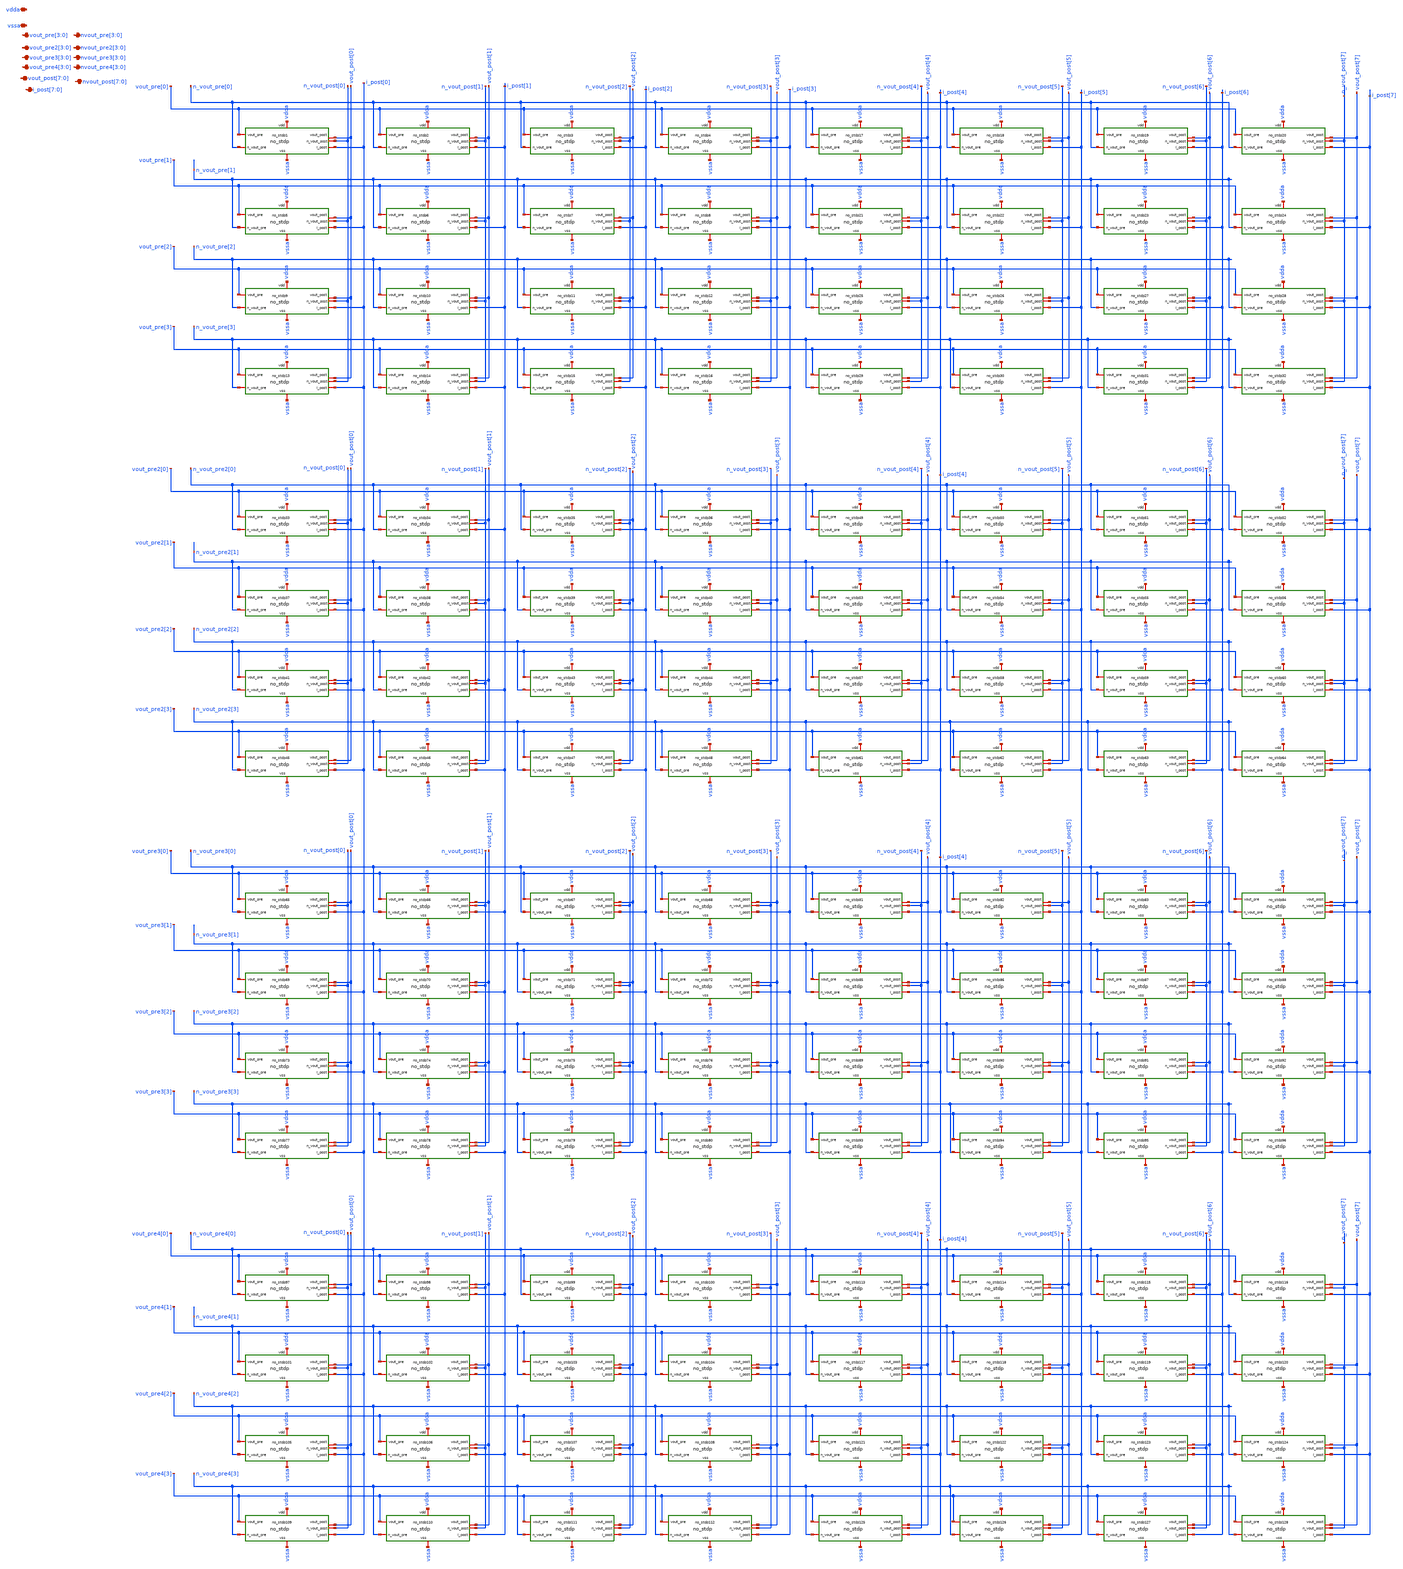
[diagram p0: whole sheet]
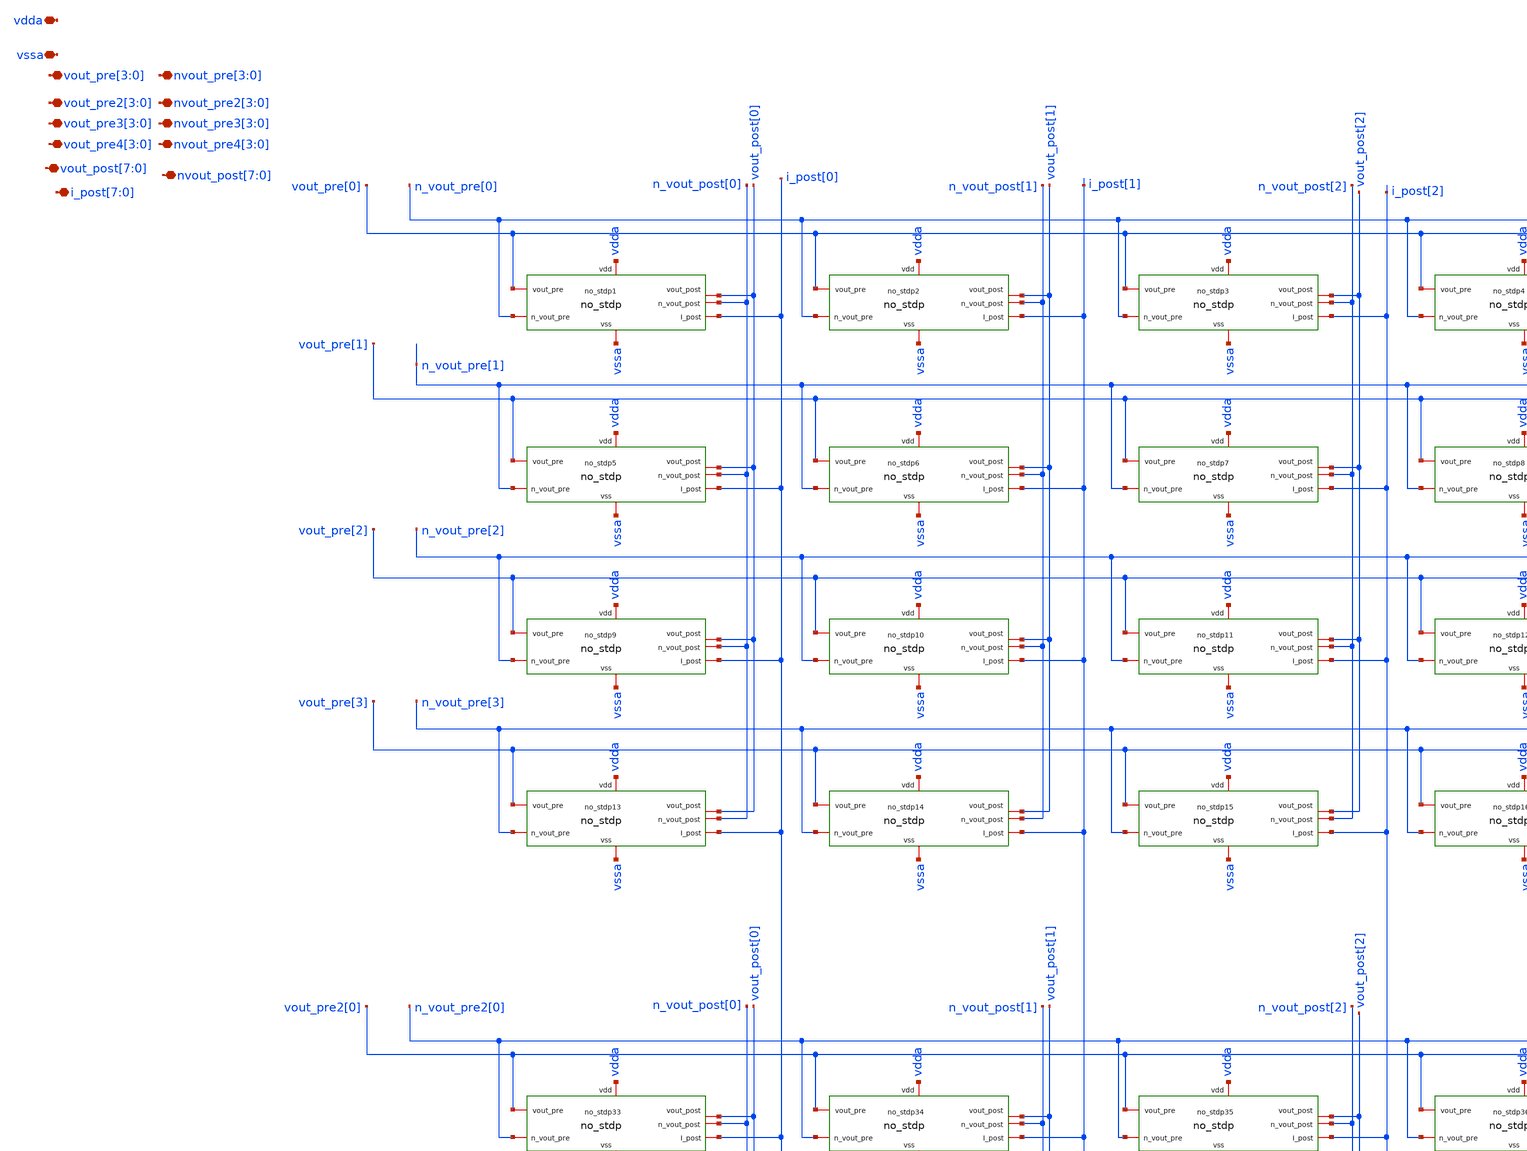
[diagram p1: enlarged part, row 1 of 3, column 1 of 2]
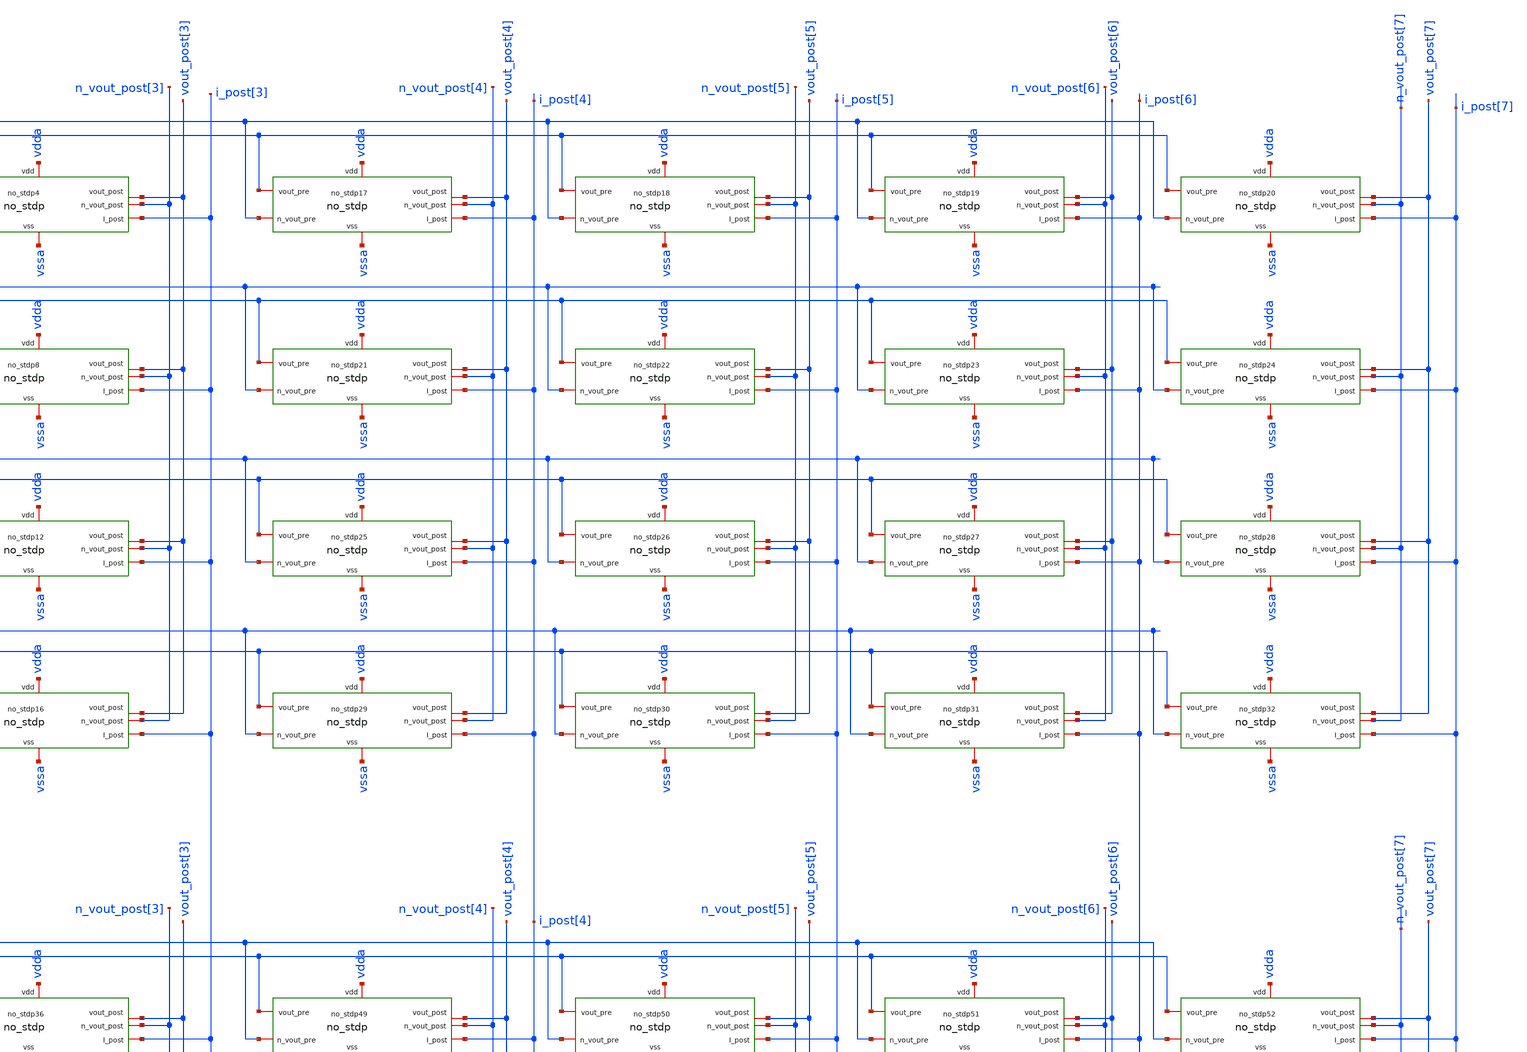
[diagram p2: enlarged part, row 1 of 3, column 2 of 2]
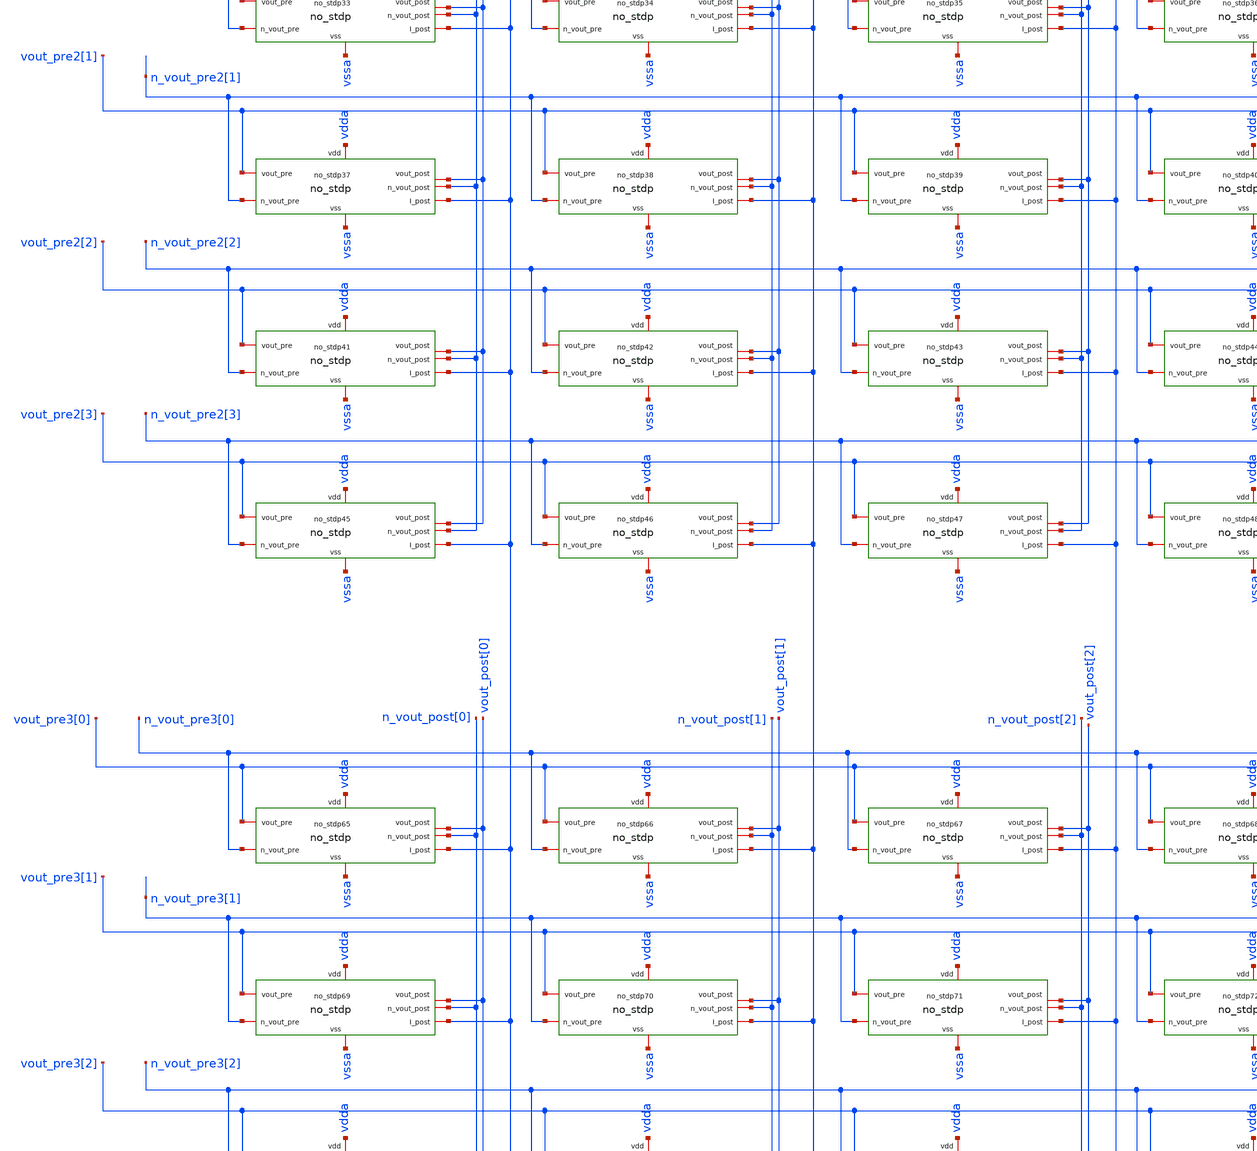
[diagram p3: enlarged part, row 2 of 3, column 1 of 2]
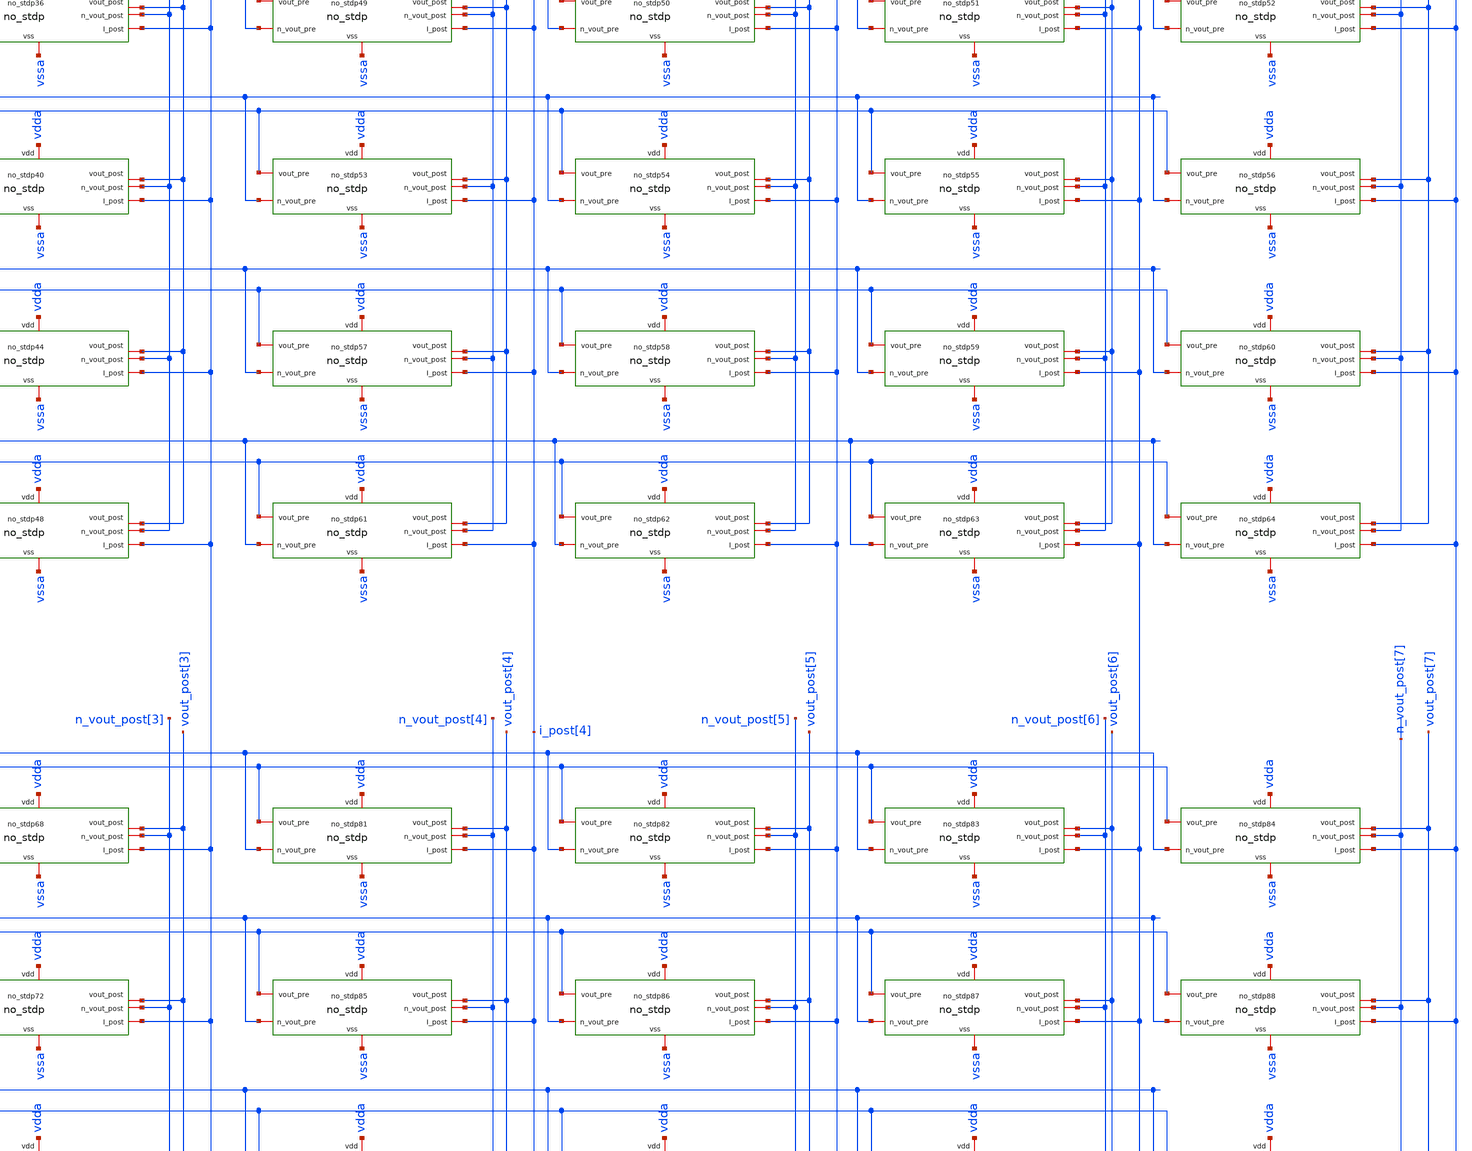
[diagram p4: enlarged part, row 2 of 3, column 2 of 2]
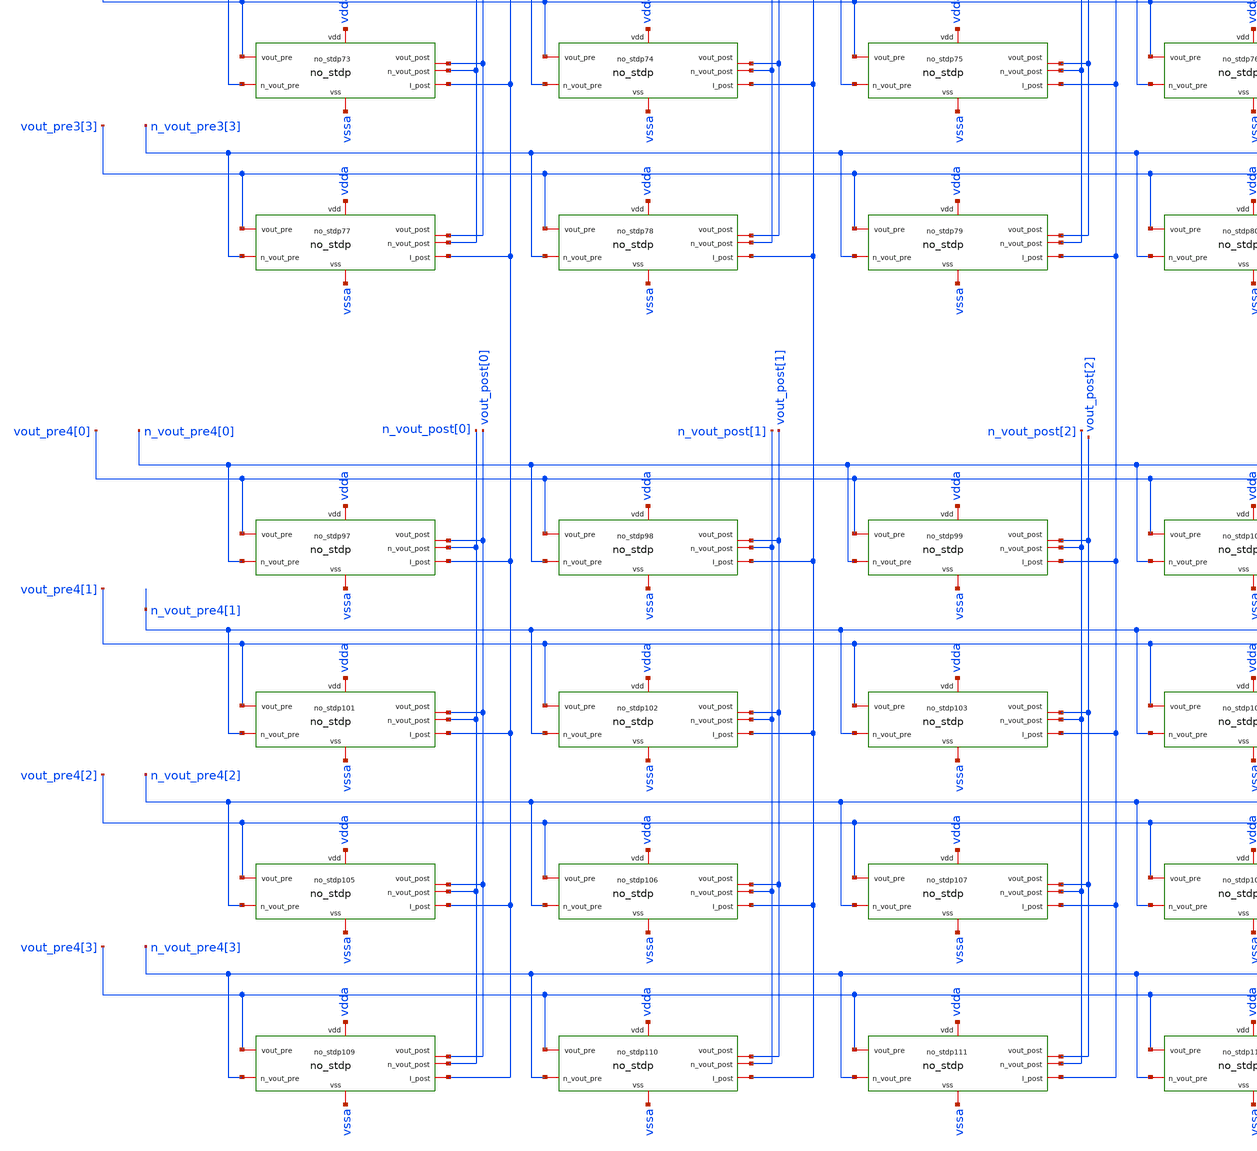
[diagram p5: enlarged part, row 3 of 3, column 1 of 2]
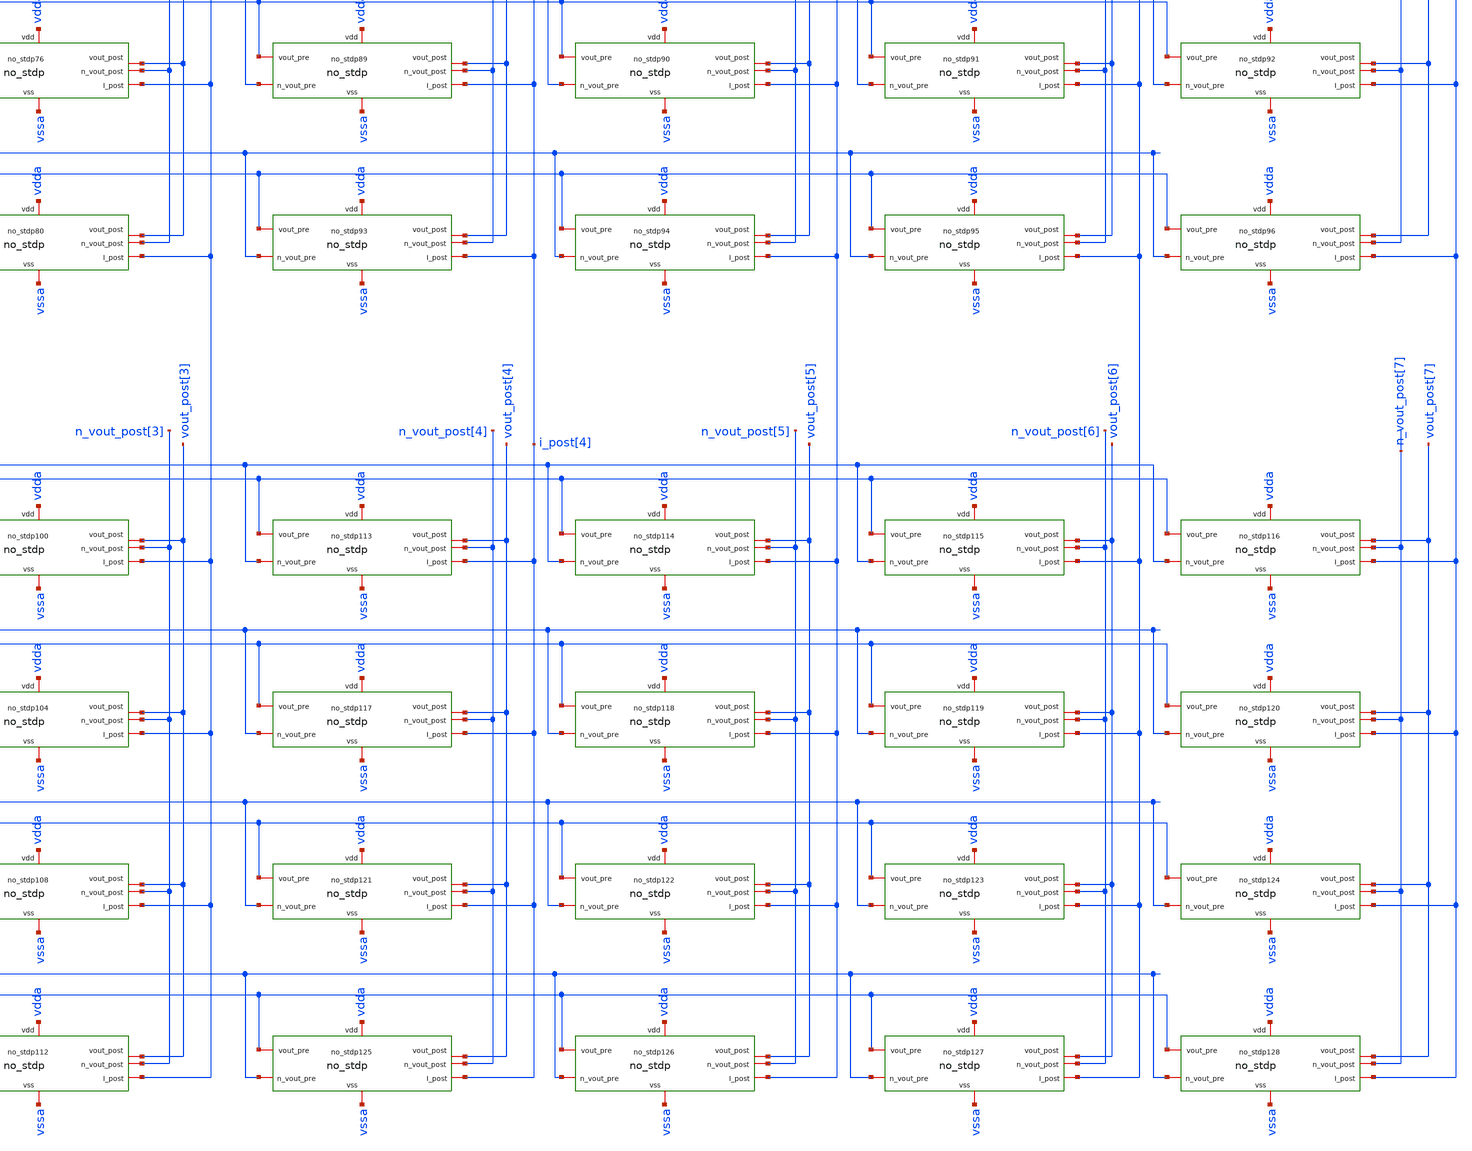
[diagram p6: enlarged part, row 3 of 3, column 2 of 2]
** sch_path: Synapse/no_stdp_4x4x8.sch
**.subckt no_stdp_4x4x8 vdda vssa vout_pre[3],vout_pre[2],vout_pre[1],vout_pre[0]
*+ vout_post[7],vout_post[6],vout_post[5],vout_post[4],vout_post[3],vout_post[2],vout_post[1],vout_post[0] i_post[7],i_post[6],i_post[5],i_post[4],i_post[3],i_post[2],i_post[1],i_post[0]
*+ vout_pre2[3],vout_pre2[2],vout_pre2[1],vout_pre2[0] vout_pre3[3],vout_pre3[2],vout_pre3[1],vout_pre3[0]
*+ vout_pre4[3],vout_pre4[2],vout_pre4[1],vout_pre4[0] nvout_pre[3],nvout_pre[2],nvout_pre[1],nvout_pre[0]
*+ nvout_pre2[3],nvout_pre2[2],nvout_pre2[1],nvout_pre2[0] nvout_pre3[3],nvout_pre3[2],nvout_pre3[1],nvout_pre3[0]
*+ nvout_pre4[3],nvout_pre4[2],nvout_pre4[1],nvout_pre4[0]
*+ nvout_post[7],nvout_post[6],nvout_post[5],nvout_post[4],nvout_post[3],nvout_post[2],nvout_post[1],nvout_post[0]
*.iopin vdda
*.iopin vssa
*.iopin vout_pre[3],vout_pre[2],vout_pre[1],vout_pre[0]
*.iopin
*+ vout_post[7],vout_post[6],vout_post[5],vout_post[4],vout_post[3],vout_post[2],vout_post[1],vout_post[0]
*.iopin i_post[7],i_post[6],i_post[5],i_post[4],i_post[3],i_post[2],i_post[1],i_post[0]
*.iopin vout_pre2[3],vout_pre2[2],vout_pre2[1],vout_pre2[0]
*.iopin vout_pre3[3],vout_pre3[2],vout_pre3[1],vout_pre3[0]
*.iopin vout_pre4[3],vout_pre4[2],vout_pre4[1],vout_pre4[0]
*.iopin nvout_pre[3],nvout_pre[2],nvout_pre[1],nvout_pre[0]
*.iopin nvout_pre2[3],nvout_pre2[2],nvout_pre2[1],nvout_pre2[0]
*.iopin nvout_pre3[3],nvout_pre3[2],nvout_pre3[1],nvout_pre3[0]
*.iopin nvout_pre4[3],nvout_pre4[2],nvout_pre4[1],nvout_pre4[0]
*.iopin
*+ nvout_post[7],nvout_post[6],nvout_post[5],nvout_post[4],nvout_post[3],nvout_post[2],nvout_post[1],nvout_post[0]
xno_stdp1 vdda vssa vout_pre[0] vout_post[0] i_post[0] n_vout_pre[0] n_vout_post[0] no_stdp
xno_stdp2 vdda vssa vout_pre[0] vout_post[1] i_post[1] n_vout_pre[0] n_vout_post[1] no_stdp
xno_stdp3 vdda vssa vout_pre[0] vout_post[2] i_post[2] n_vout_pre[0] n_vout_post[2] no_stdp
xno_stdp4 vdda vssa vout_pre[0] vout_post[3] i_post[3] n_vout_pre[0] n_vout_post[3] no_stdp
xno_stdp5 vdda vssa vout_pre[1] vout_post[0] i_post[0] n_vout_pre[1] n_vout_post[0] no_stdp
xno_stdp6 vdda vssa vout_pre[1] vout_post[1] i_post[1] n_vout_pre[1] n_vout_post[1] no_stdp
xno_stdp7 vdda vssa vout_pre[1] vout_post[2] i_post[2] n_vout_pre[1] n_vout_post[2] no_stdp
xno_stdp8 vdda vssa vout_pre[1] vout_post[3] i_post[3] n_vout_pre[1] n_vout_post[3] no_stdp
xno_stdp9 vdda vssa vout_pre[2] vout_post[0] i_post[0] n_vout_pre[2] n_vout_post[0] no_stdp
xno_stdp10 vdda vssa vout_pre[2] vout_post[1] i_post[1] n_vout_pre[2] n_vout_post[1] no_stdp
xno_stdp11 vdda vssa vout_pre[2] vout_post[2] i_post[2] n_vout_pre[2] n_vout_post[2] no_stdp
xno_stdp12 vdda vssa vout_pre[2] vout_post[3] i_post[3] n_vout_pre[2] n_vout_post[3] no_stdp
xno_stdp13 vdda vssa vout_pre[3] vout_post[0] i_post[0] n_vout_pre[3] n_vout_post[0] no_stdp
xno_stdp14 vdda vssa vout_pre[3] vout_post[1] i_post[1] n_vout_pre[3] n_vout_post[1] no_stdp
xno_stdp15 vdda vssa vout_pre[3] vout_post[2] i_post[2] n_vout_pre[3] n_vout_post[2] no_stdp
xno_stdp16 vdda vssa vout_pre[3] vout_post[3] i_post[3] n_vout_pre[3] n_vout_post[3] no_stdp
xno_stdp17 vdda vssa vout_pre[0] vout_post[4] i_post[4] n_vout_pre[0] n_vout_post[4] no_stdp
xno_stdp18 vdda vssa vout_pre[0] vout_post[5] i_post[5] n_vout_pre[0] n_vout_post[5] no_stdp
xno_stdp19 vdda vssa vout_pre[0] vout_post[6] i_post[6] n_vout_pre[0] n_vout_post[6] no_stdp
xno_stdp20 vdda vssa vout_pre[0] vout_post[7] i_post[7] n_vout_pre[0] n_vout_post[7] no_stdp
xno_stdp21 vdda vssa vout_pre[1] vout_post[4] i_post[4] n_vout_pre[1] n_vout_post[4] no_stdp
xno_stdp22 vdda vssa vout_pre[1] vout_post[5] i_post[5] n_vout_pre[1] n_vout_post[5] no_stdp
xno_stdp23 vdda vssa vout_pre[1] vout_post[6] i_post[6] n_vout_pre[1] n_vout_post[6] no_stdp
xno_stdp24 vdda vssa vout_pre[1] vout_post[7] i_post[7] n_vout_pre[1] n_vout_post[7] no_stdp
xno_stdp25 vdda vssa vout_pre[2] vout_post[4] i_post[4] n_vout_pre[2] n_vout_post[4] no_stdp
xno_stdp26 vdda vssa vout_pre[2] vout_post[5] i_post[5] n_vout_pre[2] n_vout_post[5] no_stdp
xno_stdp27 vdda vssa vout_pre[2] vout_post[6] i_post[6] n_vout_pre[2] n_vout_post[6] no_stdp
xno_stdp28 vdda vssa vout_pre[2] vout_post[7] i_post[7] n_vout_pre[2] n_vout_post[7] no_stdp
xno_stdp29 vdda vssa vout_pre[3] vout_post[4] i_post[4] n_vout_pre[3] n_vout_post[4] no_stdp
xno_stdp30 vdda vssa vout_pre[3] vout_post[5] i_post[5] n_vout_pre[3] n_vout_post[5] no_stdp
xno_stdp31 vdda vssa vout_pre[3] vout_post[6] i_post[6] n_vout_pre[3] n_vout_post[6] no_stdp
xno_stdp32 vdda vssa vout_pre[3] vout_post[7] i_post[7] n_vout_pre[3] n_vout_post[7] no_stdp
xno_stdp33 vdda vssa vout_pre2[0] vout_post[0] i_post[0] n_vout_pre2[0] n_vout_post[0] no_stdp
xno_stdp34 vdda vssa vout_pre2[0] vout_post[1] i_post[1] n_vout_pre2[0] n_vout_post[1] no_stdp
xno_stdp35 vdda vssa vout_pre2[0] vout_post[2] i_post[2] n_vout_pre2[0] n_vout_post[2] no_stdp
xno_stdp36 vdda vssa vout_pre2[0] vout_post[3] i_post[3] n_vout_pre2[0] n_vout_post[3] no_stdp
xno_stdp37 vdda vssa vout_pre2[1] vout_post[0] i_post[0] n_vout_pre2[1] n_vout_post[0] no_stdp
xno_stdp38 vdda vssa vout_pre2[1] vout_post[1] i_post[1] n_vout_pre2[1] n_vout_post[1] no_stdp
xno_stdp39 vdda vssa vout_pre2[1] vout_post[2] i_post[2] n_vout_pre2[1] n_vout_post[2] no_stdp
xno_stdp40 vdda vssa vout_pre2[1] vout_post[3] i_post[3] n_vout_pre2[1] n_vout_post[3] no_stdp
xno_stdp41 vdda vssa vout_pre2[2] vout_post[0] i_post[0] n_vout_pre2[2] n_vout_post[0] no_stdp
xno_stdp42 vdda vssa vout_pre2[2] vout_post[1] i_post[1] n_vout_pre2[2] n_vout_post[1] no_stdp
xno_stdp43 vdda vssa vout_pre2[2] vout_post[2] i_post[2] n_vout_pre2[2] n_vout_post[2] no_stdp
xno_stdp44 vdda vssa vout_pre2[2] vout_post[3] i_post[3] n_vout_pre2[2] n_vout_post[3] no_stdp
xno_stdp45 vdda vssa vout_pre2[3] vout_post[0] i_post[0] n_vout_pre2[3] n_vout_post[0] no_stdp
xno_stdp46 vdda vssa vout_pre2[3] vout_post[1] i_post[1] n_vout_pre2[3] n_vout_post[1] no_stdp
xno_stdp47 vdda vssa vout_pre2[3] vout_post[2] i_post[2] n_vout_pre2[3] n_vout_post[2] no_stdp
xno_stdp48 vdda vssa vout_pre2[3] vout_post[3] i_post[3] n_vout_pre2[3] n_vout_post[3] no_stdp
xno_stdp49 vdda vssa vout_pre2[0] vout_post[4] i_post[4] n_vout_pre2[0] n_vout_post[4] no_stdp
xno_stdp50 vdda vssa vout_pre2[0] vout_post[5] i_post[5] n_vout_pre2[0] n_vout_post[5] no_stdp
xno_stdp51 vdda vssa vout_pre2[0] vout_post[6] i_post[6] n_vout_pre2[0] n_vout_post[6] no_stdp
xno_stdp52 vdda vssa vout_pre2[0] vout_post[7] i_post[7] n_vout_pre2[0] n_vout_post[7] no_stdp
xno_stdp53 vdda vssa vout_pre2[1] vout_post[4] i_post[4] n_vout_pre2[1] n_vout_post[4] no_stdp
xno_stdp54 vdda vssa vout_pre2[1] vout_post[5] i_post[5] n_vout_pre2[1] n_vout_post[5] no_stdp
xno_stdp55 vdda vssa vout_pre2[1] vout_post[6] i_post[6] n_vout_pre2[1] n_vout_post[6] no_stdp
xno_stdp56 vdda vssa vout_pre2[1] vout_post[7] i_post[7] n_vout_pre2[1] n_vout_post[7] no_stdp
xno_stdp57 vdda vssa vout_pre2[2] vout_post[4] i_post[4] n_vout_pre2[2] n_vout_post[4] no_stdp
xno_stdp58 vdda vssa vout_pre2[2] vout_post[5] i_post[5] n_vout_pre2[2] n_vout_post[5] no_stdp
xno_stdp59 vdda vssa vout_pre2[2] vout_post[6] i_post[6] n_vout_pre2[2] n_vout_post[6] no_stdp
xno_stdp60 vdda vssa vout_pre2[2] vout_post[7] i_post[7] n_vout_pre2[2] n_vout_post[7] no_stdp
xno_stdp61 vdda vssa vout_pre2[3] vout_post[4] i_post[4] n_vout_pre2[3] n_vout_post[4] no_stdp
xno_stdp62 vdda vssa vout_pre2[3] vout_post[5] i_post[5] n_vout_pre2[3] n_vout_post[5] no_stdp
xno_stdp63 vdda vssa vout_pre2[3] vout_post[6] i_post[6] n_vout_pre2[3] n_vout_post[6] no_stdp
xno_stdp64 vdda vssa vout_pre2[3] vout_post[7] i_post[7] n_vout_pre2[3] n_vout_post[7] no_stdp
xno_stdp65 vdda vssa vout_pre3[0] vout_post[0] i_post[0] n_vout_pre3[0] n_vout_post[0] no_stdp
xno_stdp66 vdda vssa vout_pre3[0] vout_post[1] i_post[1] n_vout_pre3[0] n_vout_post[1] no_stdp
xno_stdp67 vdda vssa vout_pre3[0] vout_post[2] i_post[2] n_vout_pre3[0] n_vout_post[2] no_stdp
xno_stdp68 vdda vssa vout_pre3[0] vout_post[3] i_post[3] n_vout_pre3[0] n_vout_post[3] no_stdp
xno_stdp69 vdda vssa vout_pre3[1] vout_post[0] i_post[0] n_vout_pre3[1] n_vout_post[0] no_stdp
xno_stdp70 vdda vssa vout_pre3[1] vout_post[1] i_post[1] n_vout_pre3[1] n_vout_post[1] no_stdp
xno_stdp71 vdda vssa vout_pre3[1] vout_post[2] i_post[2] n_vout_pre3[1] n_vout_post[2] no_stdp
xno_stdp72 vdda vssa vout_pre3[1] vout_post[3] i_post[3] n_vout_pre3[1] n_vout_post[3] no_stdp
xno_stdp73 vdda vssa vout_pre3[2] vout_post[0] i_post[0] n_vout_pre3[2] n_vout_post[0] no_stdp
xno_stdp74 vdda vssa vout_pre3[2] vout_post[1] i_post[1] n_vout_pre3[2] n_vout_post[1] no_stdp
xno_stdp75 vdda vssa vout_pre3[2] vout_post[2] i_post[2] n_vout_pre3[2] n_vout_post[2] no_stdp
xno_stdp76 vdda vssa vout_pre3[2] vout_post[3] i_post[3] n_vout_pre3[2] n_vout_post[3] no_stdp
xno_stdp77 vdda vssa vout_pre3[3] vout_post[0] i_post[0] n_vout_pre3[3] n_vout_post[0] no_stdp
xno_stdp78 vdda vssa vout_pre3[3] vout_post[1] i_post[1] n_vout_pre3[3] n_vout_post[1] no_stdp
xno_stdp79 vdda vssa vout_pre3[3] vout_post[2] i_post[2] n_vout_pre3[3] n_vout_post[2] no_stdp
xno_stdp80 vdda vssa vout_pre3[3] vout_post[3] i_post[3] n_vout_pre3[3] n_vout_post[3] no_stdp
xno_stdp81 vdda vssa vout_pre3[0] vout_post[4] i_post[4] n_vout_pre3[0] n_vout_post[4] no_stdp
xno_stdp82 vdda vssa vout_pre3[0] vout_post[5] i_post[5] n_vout_pre3[0] n_vout_post[5] no_stdp
xno_stdp83 vdda vssa vout_pre3[0] vout_post[6] i_post[6] n_vout_pre3[0] n_vout_post[6] no_stdp
xno_stdp84 vdda vssa vout_pre3[0] vout_post[7] i_post[7] n_vout_pre3[0] n_vout_post[7] no_stdp
xno_stdp85 vdda vssa vout_pre3[1] vout_post[4] i_post[4] n_vout_pre3[1] n_vout_post[4] no_stdp
xno_stdp86 vdda vssa vout_pre3[1] vout_post[5] i_post[5] n_vout_pre3[1] n_vout_post[5] no_stdp
xno_stdp87 vdda vssa vout_pre3[1] vout_post[6] i_post[6] n_vout_pre3[1] n_vout_post[6] no_stdp
xno_stdp88 vdda vssa vout_pre3[1] vout_post[7] i_post[7] n_vout_pre3[1] n_vout_post[7] no_stdp
xno_stdp89 vdda vssa vout_pre3[2] vout_post[4] i_post[4] n_vout_pre3[2] n_vout_post[4] no_stdp
xno_stdp90 vdda vssa vout_pre3[2] vout_post[5] i_post[5] n_vout_pre3[2] n_vout_post[5] no_stdp
xno_stdp91 vdda vssa vout_pre3[2] vout_post[6] i_post[6] n_vout_pre3[2] n_vout_post[6] no_stdp
xno_stdp92 vdda vssa vout_pre3[2] vout_post[7] i_post[7] n_vout_pre3[2] n_vout_post[7] no_stdp
xno_stdp93 vdda vssa vout_pre3[3] vout_post[4] i_post[4] n_vout_pre3[3] n_vout_post[4] no_stdp
xno_stdp94 vdda vssa vout_pre3[3] vout_post[5] i_post[5] n_vout_pre3[3] n_vout_post[5] no_stdp
xno_stdp95 vdda vssa vout_pre3[3] vout_post[6] i_post[6] n_vout_pre3[3] n_vout_post[6] no_stdp
xno_stdp96 vdda vssa vout_pre3[3] vout_post[7] i_post[7] n_vout_pre3[3] n_vout_post[7] no_stdp
xno_stdp97 vdda vssa vout_pre4[0] vout_post[0] i_post[0] n_vout_pre4[0] n_vout_post[0] no_stdp
xno_stdp98 vdda vssa vout_pre4[0] vout_post[1] i_post[1] n_vout_pre4[0] n_vout_post[1] no_stdp
xno_stdp99 vdda vssa vout_pre4[0] vout_post[2] i_post[2] n_vout_pre4[0] n_vout_post[2] no_stdp
xno_stdp100 vdda vssa vout_pre4[0] vout_post[3] i_post[3] n_vout_pre4[0] n_vout_post[3] no_stdp
xno_stdp101 vdda vssa vout_pre4[1] vout_post[0] i_post[0] n_vout_pre4[1] n_vout_post[0] no_stdp
xno_stdp102 vdda vssa vout_pre4[1] vout_post[1] i_post[1] n_vout_pre4[1] n_vout_post[1] no_stdp
xno_stdp103 vdda vssa vout_pre4[1] vout_post[2] i_post[2] n_vout_pre4[1] n_vout_post[2] no_stdp
xno_stdp104 vdda vssa vout_pre4[1] vout_post[3] i_post[3] n_vout_pre4[1] n_vout_post[3] no_stdp
xno_stdp105 vdda vssa vout_pre4[2] vout_post[0] i_post[0] n_vout_pre4[2] n_vout_post[0] no_stdp
xno_stdp106 vdda vssa vout_pre4[2] vout_post[1] i_post[1] n_vout_pre4[2] n_vout_post[1] no_stdp
xno_stdp107 vdda vssa vout_pre4[2] vout_post[2] i_post[2] n_vout_pre4[2] n_vout_post[2] no_stdp
xno_stdp108 vdda vssa vout_pre4[2] vout_post[3] i_post[3] n_vout_pre4[2] n_vout_post[3] no_stdp
xno_stdp109 vdda vssa vout_pre4[3] vout_post[0] i_post[0] n_vout_pre4[3] n_vout_post[0] no_stdp
xno_stdp110 vdda vssa vout_pre4[3] vout_post[1] i_post[1] n_vout_pre4[3] n_vout_post[1] no_stdp
xno_stdp111 vdda vssa vout_pre4[3] vout_post[2] i_post[2] n_vout_pre4[3] n_vout_post[2] no_stdp
xno_stdp112 vdda vssa vout_pre4[3] vout_post[3] i_post[3] n_vout_pre4[3] n_vout_post[3] no_stdp
xno_stdp113 vdda vssa vout_pre4[0] vout_post[4] i_post[4] n_vout_pre4[0] n_vout_post[4] no_stdp
xno_stdp114 vdda vssa vout_pre4[0] vout_post[5] i_post[5] n_vout_pre4[0] n_vout_post[5] no_stdp
xno_stdp115 vdda vssa vout_pre4[0] vout_post[6] i_post[6] n_vout_pre4[0] n_vout_post[6] no_stdp
xno_stdp116 vdda vssa vout_pre4[0] vout_post[7] i_post[7] n_vout_pre4[0] n_vout_post[7] no_stdp
xno_stdp117 vdda vssa vout_pre4[1] vout_post[4] i_post[4] n_vout_pre4[1] n_vout_post[4] no_stdp
xno_stdp118 vdda vssa vout_pre4[1] vout_post[5] i_post[5] n_vout_pre4[1] n_vout_post[5] no_stdp
xno_stdp119 vdda vssa vout_pre4[1] vout_post[6] i_post[6] n_vout_pre4[1] n_vout_post[6] no_stdp
xno_stdp120 vdda vssa vout_pre4[1] vout_post[7] i_post[7] n_vout_pre4[1] n_vout_post[7] no_stdp
xno_stdp121 vdda vssa vout_pre4[2] vout_post[4] i_post[4] n_vout_pre4[2] n_vout_post[4] no_stdp
xno_stdp122 vdda vssa vout_pre4[2] vout_post[5] i_post[5] n_vout_pre4[2] n_vout_post[5] no_stdp
xno_stdp123 vdda vssa vout_pre4[2] vout_post[6] i_post[6] n_vout_pre4[2] n_vout_post[6] no_stdp
xno_stdp124 vdda vssa vout_pre4[2] vout_post[7] i_post[7] n_vout_pre4[2] n_vout_post[7] no_stdp
xno_stdp125 vdda vssa vout_pre4[3] vout_post[4] i_post[4] n_vout_pre4[3] n_vout_post[4] no_stdp
xno_stdp126 vdda vssa vout_pre4[3] vout_post[5] i_post[5] n_vout_pre4[3] n_vout_post[5] no_stdp
xno_stdp127 vdda vssa vout_pre4[3] vout_post[6] i_post[6] n_vout_pre4[3] n_vout_post[6] no_stdp
xno_stdp128 vdda vssa vout_pre4[3] vout_post[7] i_post[7] n_vout_pre4[3] n_vout_post[7] no_stdp
**.ends

* expanding   symbol:  Synapse/no_stdp.sym # of pins=7
** sym_path: Synapse/no_stdp.sym
** sch_path: Synapse/no_stdp.sch
.subckt no_stdp vdd vss vout_pre vout_post I_post n_vout_pre n_vout_post
*.iopin vdd
*.iopin vss
*.iopin vout_post
*.iopin vout_pre
*.iopin I_post
*.iopin n_vout_post
*.iopin n_vout_pre
XM3 be vout_post vss vss sky130_fd_pr__nfet_01v8 L=0.15 W=0.5 nf=1 ad='int((nf+1)/2) * W/nf * 0.29' as='int((nf+2)/2) * W/nf * 0.29'
+ pd='2*int((nf+1)/2) * (W/nf + 0.29)' ps='2*int((nf+2)/2) * (W/nf + 0.29)' nrd='0.29 / W' nrs='0.29 / W'
+ sa=0 sb=0 sd=0 mult=1 m=1
XM4 te vout_pre vss vss sky130_fd_pr__nfet_01v8 L=0.15 W=0.5 nf=1 ad='int((nf+1)/2) * W/nf * 0.29' as='int((nf+2)/2) * W/nf * 0.29'
+ pd='2*int((nf+1)/2) * (W/nf + 0.29)' ps='2*int((nf+2)/2) * (W/nf + 0.29)' nrd='0.29 / W' nrs='0.29 / W'
+ sa=0 sb=0 sd=0 mult=1 m=1
XM14 net2 net1 vdd vdd sky130_fd_pr__pfet_01v8 L=0.15 W=0.5 nf=1 ad='int((nf+1)/2) * W/nf * 0.29' as='int((nf+2)/2) * W/nf * 0.29'
+ pd='2*int((nf+1)/2) * (W/nf + 0.29)' ps='2*int((nf+2)/2) * (W/nf + 0.29)' nrd='0.29 / W' nrs='0.29 / W'
+ sa=0 sb=0 sd=0 mult=1 m=1
XM15 net1 net1 vdd vdd sky130_fd_pr__pfet_01v8 L=0.15 W=1 nf=1 ad='int((nf+1)/2) * W/nf * 0.29' as='int((nf+2)/2) * W/nf * 0.29'
+ pd='2*int((nf+1)/2) * (W/nf + 0.29)' ps='2*int((nf+2)/2) * (W/nf + 0.29)' nrd='0.29 / W' nrs='0.29 / W'
+ sa=0 sb=0 sd=0 mult=1 m=1
XM1 te n_vout_post net1 vss sky130_fd_pr__pfet_01v8 L=0.15 W=1 nf=1 ad='int((nf+1)/2) * W/nf * 0.29'
+ as='int((nf+2)/2) * W/nf * 0.29' pd='2*int((nf+1)/2) * (W/nf + 0.29)' ps='2*int((nf+2)/2) * (W/nf + 0.29)'
+ nrd='0.29 / W' nrs='0.29 / W' sa=0 sb=0 sd=0 mult=1 m=1
XM2 be n_vout_pre net1 vss sky130_fd_pr__pfet_01v8 L=0.15 W=1 nf=1 ad='int((nf+1)/2) * W/nf * 0.29' as='int((nf+2)/2) * W/nf * 0.29'
+ pd='2*int((nf+1)/2) * (W/nf + 0.29)' ps='2*int((nf+2)/2) * (W/nf + 0.29)' nrd='0.29 / W' nrs='0.29 / W'
+ sa=0 sb=0 sd=0 mult=1 m=1
XM6 I_post net1 net2 vdd sky130_fd_pr__pfet_01v8 L=0.15 W=0.5 nf=1 ad='int((nf+1)/2) * W/nf * 0.29' as='int((nf+2)/2) * W/nf * 0.29'
+ pd='2*int((nf+1)/2) * (W/nf + 0.29)' ps='2*int((nf+2)/2) * (W/nf + 0.29)' nrd='0.29 / W' nrs='0.29 / W'
+ sa=0 sb=0 sd=0 mult=1 m=1
R1 be te 'AGAUSS((3300000)/2,500000, 1)' m=1
.ends

.end
